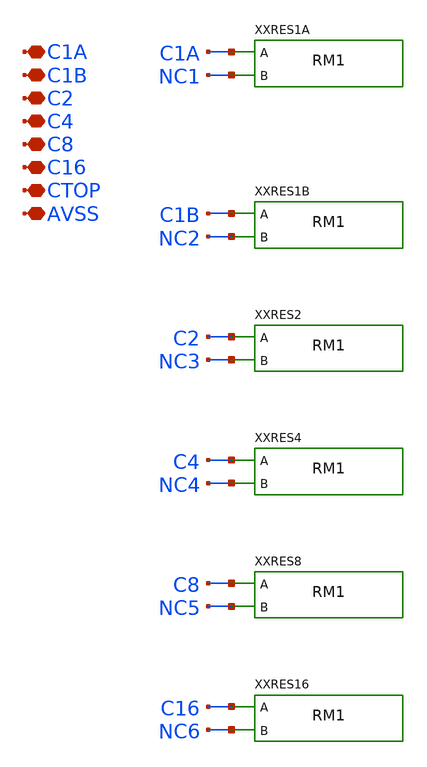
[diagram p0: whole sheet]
** sch_path: tests/transpile/SAR9B/CAP32C_CV.sch
**.subckt CAP32C_CV C1A C1B C2 C4 C8 C16 CTOP AVSS
*.iopin C1A
*.iopin C1B
*.iopin C2
*.iopin C4
*.iopin C8
*.iopin C16
*.iopin CTOP
*.iopin AVSS
XXRES1A C1A NC1 RM1
XXRES1B C1B NC2 RM1
XXRES2 C2 NC3 RM1
XXRES4 C4 NC4 RM1
XXRES8 C8 NC5 RM1
XXRES16 C16 NC6 RM1
**.ends

* expanding   symbol:  SAR9B/RM1.sym # of pins=2
** sym_path: tests/transpile/SAR9B/RM1.sym
** sch_path: tests/transpile/SAR9B/RM1.sch
.subckt RM1 A B
*.iopin A
*.iopin B
R1 A B (value) m=1
.ends

.end
